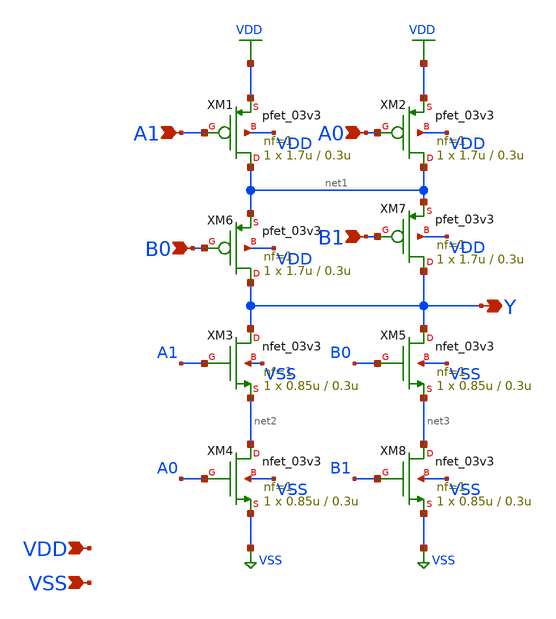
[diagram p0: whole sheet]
** sch_path: gf180mcu_osu_sc_gp12t3v3/xschem/gf180mcu_osu_sc_gp12t3v3__aoi22_1.sch
**.subckt gf180mcu_osu_sc_gp12t3v3__aoi22_1 A1 A0 B0 B1 Y VDD VSS
*.ipin A1
*.ipin A0
*.ipin B0
*.ipin B1
*.opin Y
*.ipin VDD
*.ipin VSS
XM1 net1 A1 VDD VDD pfet_03v3 L=0.3u W=1.7u nf=1 ad='int((nf+1)/2) * W/nf * 0.18u' as='int((nf+2)/2) * W/nf * 0.18u'
+ pd='2*int((nf+1)/2) * (W/nf + 0.18u)' ps='2*int((nf+2)/2) * (W/nf + 0.18u)' nrd='0.18u / W' nrs='0.18u / W'
+ sa=0 sb=0 sd=0 m=1
XM2 net1 A0 VDD VDD pfet_03v3 L=0.3u W=1.7u nf=1 ad='int((nf+1)/2) * W/nf * 0.18u' as='int((nf+2)/2) * W/nf * 0.18u'
+ pd='2*int((nf+1)/2) * (W/nf + 0.18u)' ps='2*int((nf+2)/2) * (W/nf + 0.18u)' nrd='0.18u / W' nrs='0.18u / W'
+ sa=0 sb=0 sd=0 m=1
XM3 Y A1 net2 VSS nfet_03v3 L=0.3u W=0.85u nf=1 ad='int((nf+1)/2) * W/nf * 0.18u' as='int((nf+2)/2) * W/nf * 0.18u'
+ pd='2*int((nf+1)/2) * (W/nf + 0.18u)' ps='2*int((nf+2)/2) * (W/nf + 0.18u)' nrd='0.18u / W' nrs='0.18u / W'
+ sa=0 sb=0 sd=0 m=1
XM4 net2 A0 VSS VSS nfet_03v3 L=0.3u W=0.85u nf=1 ad='int((nf+1)/2) * W/nf * 0.18u' as='int((nf+2)/2) * W/nf * 0.18u'
+ pd='2*int((nf+1)/2) * (W/nf + 0.18u)' ps='2*int((nf+2)/2) * (W/nf + 0.18u)' nrd='0.18u / W' nrs='0.18u / W'
+ sa=0 sb=0 sd=0 m=1
XM5 Y B0 net3 VSS nfet_03v3 L=0.3u W=0.85u nf=1 ad='int((nf+1)/2) * W/nf * 0.18u' as='int((nf+2)/2) * W/nf * 0.18u'
+ pd='2*int((nf+1)/2) * (W/nf + 0.18u)' ps='2*int((nf+2)/2) * (W/nf + 0.18u)' nrd='0.18u / W' nrs='0.18u / W'
+ sa=0 sb=0 sd=0 m=1
XM6 Y B0 net1 VDD pfet_03v3 L=0.3u W=1.7u nf=1 ad='int((nf+1)/2) * W/nf * 0.18u' as='int((nf+2)/2) * W/nf * 0.18u'
+ pd='2*int((nf+1)/2) * (W/nf + 0.18u)' ps='2*int((nf+2)/2) * (W/nf + 0.18u)' nrd='0.18u / W' nrs='0.18u / W'
+ sa=0 sb=0 sd=0 m=1
XM7 Y B1 net1 VDD pfet_03v3 L=0.3u W=1.7u nf=1 ad='int((nf+1)/2) * W/nf * 0.18u' as='int((nf+2)/2) * W/nf * 0.18u'
+ pd='2*int((nf+1)/2) * (W/nf + 0.18u)' ps='2*int((nf+2)/2) * (W/nf + 0.18u)' nrd='0.18u / W' nrs='0.18u / W'
+ sa=0 sb=0 sd=0 m=1
XM8 net3 B1 VSS VSS nfet_03v3 L=0.3u W=0.85u nf=1 ad='int((nf+1)/2) * W/nf * 0.18u' as='int((nf+2)/2) * W/nf * 0.18u'
+ pd='2*int((nf+1)/2) * (W/nf + 0.18u)' ps='2*int((nf+2)/2) * (W/nf + 0.18u)' nrd='0.18u / W' nrs='0.18u / W'
+ sa=0 sb=0 sd=0 m=1
**.ends
.GLOBAL VDD
.GLOBAL VSS
.end
